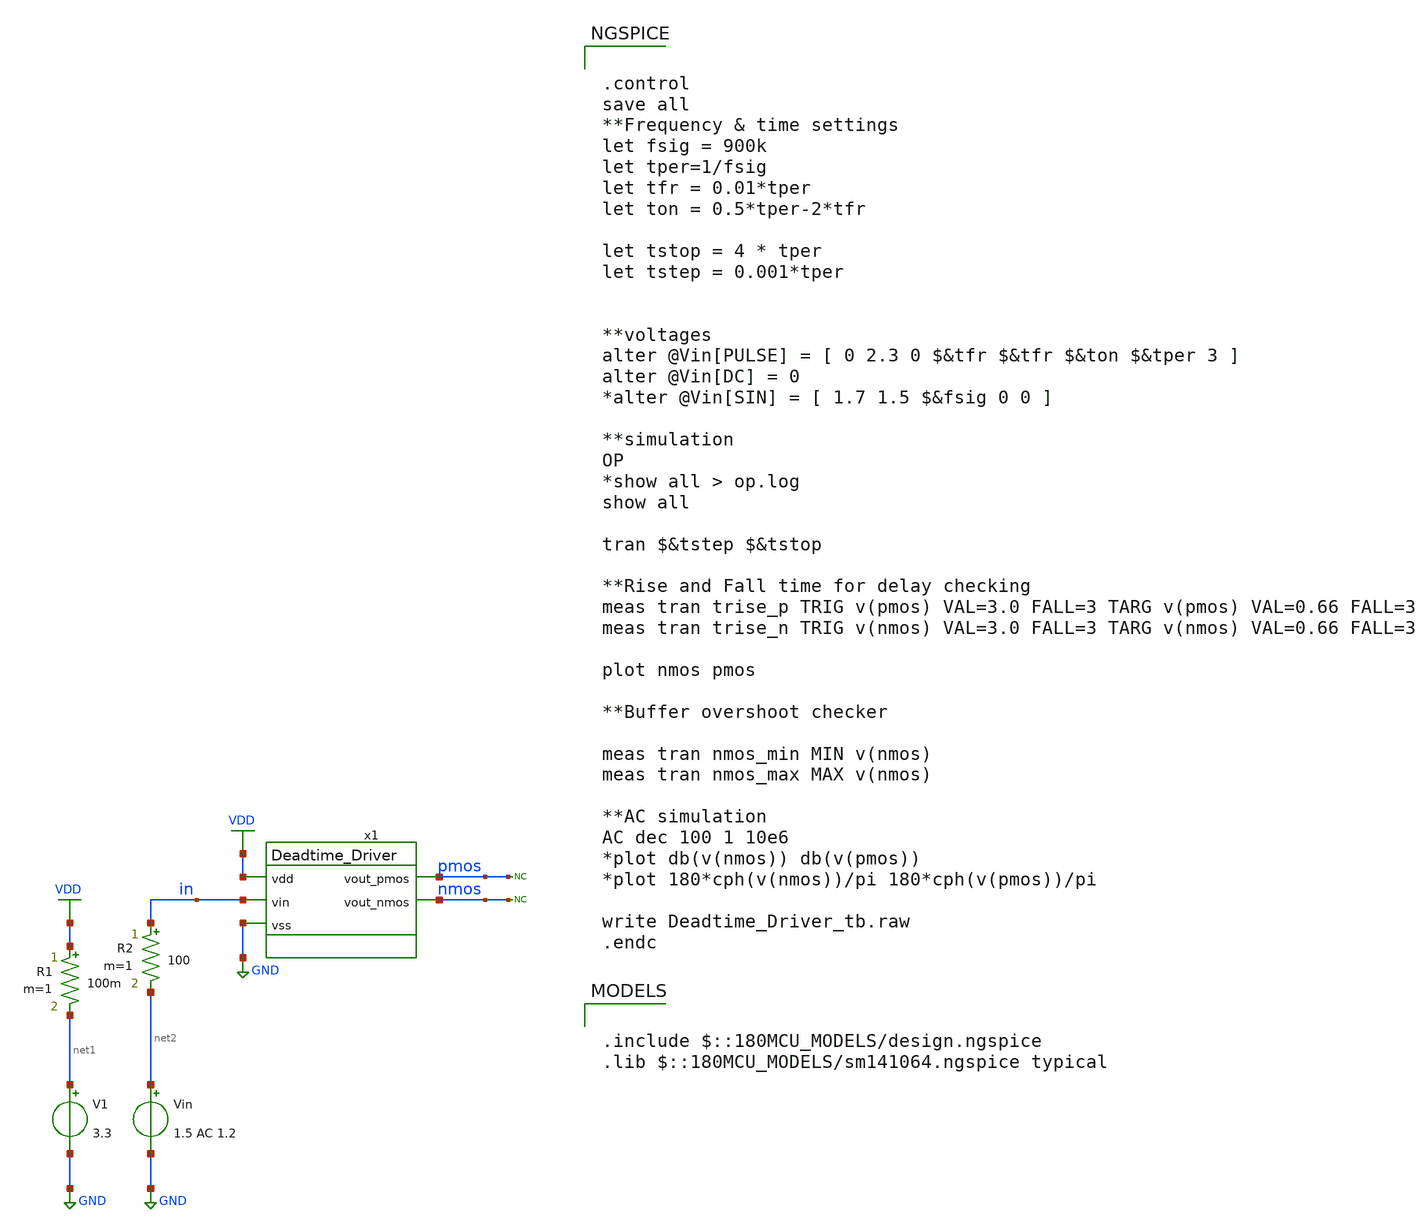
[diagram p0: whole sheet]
** sch_path: designs/libs/tb_analog/tb_Deadtime_Driver/tb_deadtime_driver.sch
**.subckt tb_deadtime_driver
V1 net1 GND 3.3
Vin net2 GND 1.5 AC 1.2
R1 VDD net1 100m m=1
R2 in net2 100 m=1
* noconn pmos
* noconn nmos
x1 VDD pmos in nmos GND Deadtime_Driver
**** begin user architecture code


.control
save all
**Frequency & time settings
let fsig = 900k
let tper=1/fsig
let tfr = 0.01*tper
let ton = 0.5*tper-2*tfr

let tstop = 4 * tper
let tstep = 0.001*tper


**voltages
alter @Vin[PULSE] = [ 0 2.3 0 $&tfr $&tfr $&ton $&tper 3 ]
alter @Vin[DC] = 0
*alter @Vin[SIN] = [ 1.7 1.5 $&fsig 0 0 ]

**simulation
OP
*show all > op.log
show all

tran $&tstep $&tstop

**Rise and Fall time for delay checking
meas tran trise_p TRIG v(pmos) VAL=3.0 FALL=3 TARG v(pmos) VAL=0.66 FALL=3
meas tran trise_n TRIG v(nmos) VAL=3.0 FALL=3 TARG v(nmos) VAL=0.66 FALL=3

plot nmos pmos

**Buffer overshoot checker

meas tran nmos_min MIN v(nmos)
meas tran nmos_max MAX v(nmos)

**AC simulation
AC dec 100 1 10e6
*plot db(v(nmos)) db(v(pmos))
*plot 180*cph(v(nmos))/pi 180*cph(v(pmos))/pi

write Deadtime_Driver_tb.raw
.endc



.include $::180MCU_MODELS/design.ngspice
.lib $::180MCU_MODELS/sm141064.ngspice typical

**** end user architecture code
**.ends
.GLOBAL GND
.GLOBAL VDD
.end
